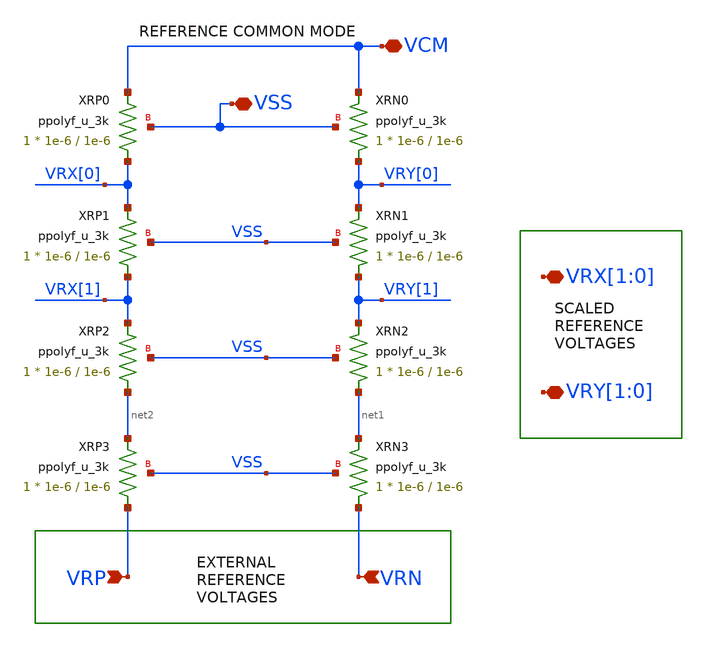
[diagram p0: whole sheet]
** sch_path: designs/sar_adc/dac/rdac/xschem/rdac.sch
**.subckt rdac VRN VRP VCM VRY[1],VRY[0] VRX[1],VRX[0] VSS
*.ipin VRN
*.ipin VRP
*.iopin VCM
*.iopin VRY[1],VRY[0]
*.iopin VRX[1],VRX[0]
*.iopin VSS
XRN0 VRY[0] VCM VSS ppolyf_u_3k r_width=1e-6 r_length=1e-6 m=1
XRN1 VRY[1] VRY[0] VSS ppolyf_u_3k r_width=1e-6 r_length=1e-6 m=1
XRN2 net1 VRY[1] VSS ppolyf_u_3k r_width=1e-6 r_length=1e-6 m=1
XRN3 VRN net1 VSS ppolyf_u_3k r_width=1e-6 r_length=1e-6 m=1
XRP0 VRX[0] VCM VSS ppolyf_u_3k r_width=1e-6 r_length=1e-6 m=1
XRP1 VRX[1] VRX[0] VSS ppolyf_u_3k r_width=1e-6 r_length=1e-6 m=1
XRP2 net2 VRX[1] VSS ppolyf_u_3k r_width=1e-6 r_length=1e-6 m=1
XRP3 VRP net2 VSS ppolyf_u_3k r_width=1e-6 r_length=1e-6 m=1
**.ends
.end
